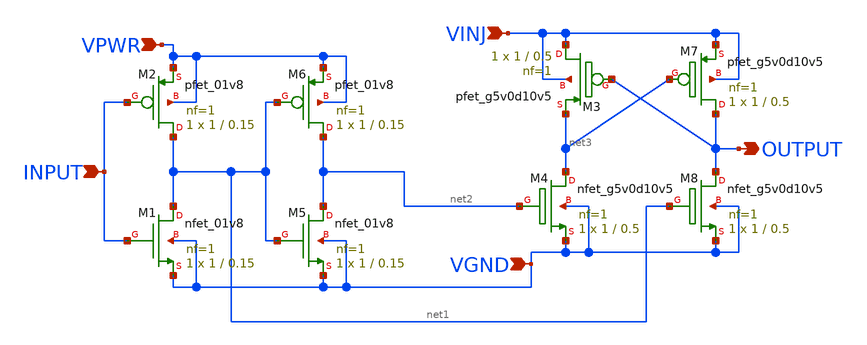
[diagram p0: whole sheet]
** sch_path: sky130_cells/ChargePump/StepupDigital.sch
**.subckt StepupDigital INPUT VPWR VINJ VGND OUTPUT
*.ipin INPUT
*.ipin VPWR
*.ipin VINJ
*.ipin VGND
*.opin OUTPUT
XM2 net1 INPUT VPWR VPWR sky130_fd_pr__pfet_01v8 L=0.15 W=1 nf=1 ad='int((nf+1)/2) * W/nf * 0.29' as='int((nf+2)/2) * W/nf * 0.29'
+ pd='2*int((nf+1)/2) * (W/nf + 0.29)' ps='2*int((nf+2)/2) * (W/nf + 0.29)' nrd='0.29 / W' nrs='0.29 / W'
+ sa=0 sb=0 sd=0 mult=1 m=1
XM6 net2 net1 VPWR VPWR sky130_fd_pr__pfet_01v8 L=0.15 W=1 nf=1 ad='int((nf+1)/2) * W/nf * 0.29' as='int((nf+2)/2) * W/nf * 0.29'
+ pd='2*int((nf+1)/2) * (W/nf + 0.29)' ps='2*int((nf+2)/2) * (W/nf + 0.29)' nrd='0.29 / W' nrs='0.29 / W'
+ sa=0 sb=0 sd=0 mult=1 m=1
XM1 net1 INPUT VGND VGND sky130_fd_pr__nfet_01v8 L=0.15 W=1 nf=1 ad='int((1 + 1)/2) * 1 / 1 * 0.29' as='int((1 + 2)/2) * 1 / 1 * 0.29'
+ pd='2*int((1 + 1)/2) * (1 / 1 + 0.29)' ps='2*int((1 + 2)/2) * (1 / 1 + 0.29)' nrd='0.29 / 1 ' nrs='0.29 / 1 '
+ sa=0 sb=0 sd=0 mult=1 m=1
XM5 net2 net1 VGND VGND sky130_fd_pr__nfet_01v8 L=0.15 W=1 nf=1 ad='int((1 + 1)/2) * 1 / 1 * 0.29' as='int((1 + 2)/2) * 1 / 1 * 0.29'
+ pd='2*int((1 + 1)/2) * (1 / 1 + 0.29)' ps='2*int((1 + 2)/2) * (1 / 1 + 0.29)' nrd='0.29 / 1 ' nrs='0.29 / 1 '
+ sa=0 sb=0 sd=0 mult=1 m=1
XM4 net3 net2 VGND VGND sky130_fd_pr__nfet_g5v0d10v5 L=0.5 W=1 nf=1 ad='int((1 + 1)/2) * 1 / 1 * 0.29'
+ as='int((1 + 2)/2) * 1 / 1 * 0.29' pd='2*int((1 + 1)/2) * (1 / 1 + 0.29)' ps='2*int((1 + 2)/2) * (1 / 1 + 0.29)'
+ nrd='0.29 / 1 ' nrs='0.29 / 1 ' sa=0 sb=0 sd=0 mult=1 m=1
XM8 OUTPUT net1 VGND VGND sky130_fd_pr__nfet_g5v0d10v5 L=0.5 W=1 nf=1 ad='int((1 + 1)/2) * 1 / 1 * 0.29'
+ as='int((1 + 2)/2) * 1 / 1 * 0.29' pd='2*int((1 + 1)/2) * (1 / 1 + 0.29)' ps='2*int((1 + 2)/2) * (1 / 1 + 0.29)'
+ nrd='0.29 / 1 ' nrs='0.29 / 1 ' sa=0 sb=0 sd=0 mult=1 m=1
XM3 VINJ OUTPUT net3 VINJ sky130_fd_pr__pfet_g5v0d10v5 L=0.5 W=1 nf=1 ad='int((1 + 1)/2) * 1 / 1 * 0.29'
+ as='int((1 + 2)/2) * 1 / 1 * 0.29' pd='2*int((1 + 1)/2) * (1 / 1 + 0.29)' ps='2*int((1 + 2)/2) * (1 / 1 + 0.29)'
+ nrd='0.29 / 1 ' nrs='0.29 / 1 ' sa=0 sb=0 sd=0 mult=1 m=1
XM7 OUTPUT net3 VINJ VINJ sky130_fd_pr__pfet_g5v0d10v5 L=0.5 W=1 nf=1 ad='int((1 + 1)/2) * 1 / 1 * 0.29'
+ as='int((1 + 2)/2) * 1 / 1 * 0.29' pd='2*int((1 + 1)/2) * (1 / 1 + 0.29)' ps='2*int((1 + 2)/2) * (1 / 1 + 0.29)'
+ nrd='0.29 / 1 ' nrs='0.29 / 1 ' sa=0 sb=0 sd=0 mult=1 m=1
**.ends
.end
